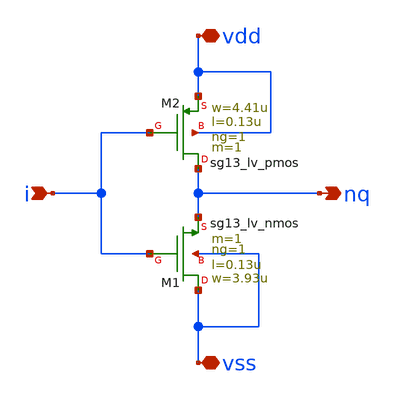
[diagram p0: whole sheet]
** sch_path: ihp-sg13g2/libs.ref/sg13g2_io/xschem/sg13g2_ioinv_x1.sch
**.subckt sg13g2_ioinv_x1 i nq vss vdd
*.ipin i
*.opin nq
*.iopin vss
*.iopin vdd
XM1 vss i nq vss sg13_lv_nmos w=3.93u l=0.13u ng=1 m=1 mm_ok=1
XM2 nq i vdd vdd sg13_lv_pmos w=4.41u l=0.13u ng=1 m=1 mm_ok=1
**.ends
.end
